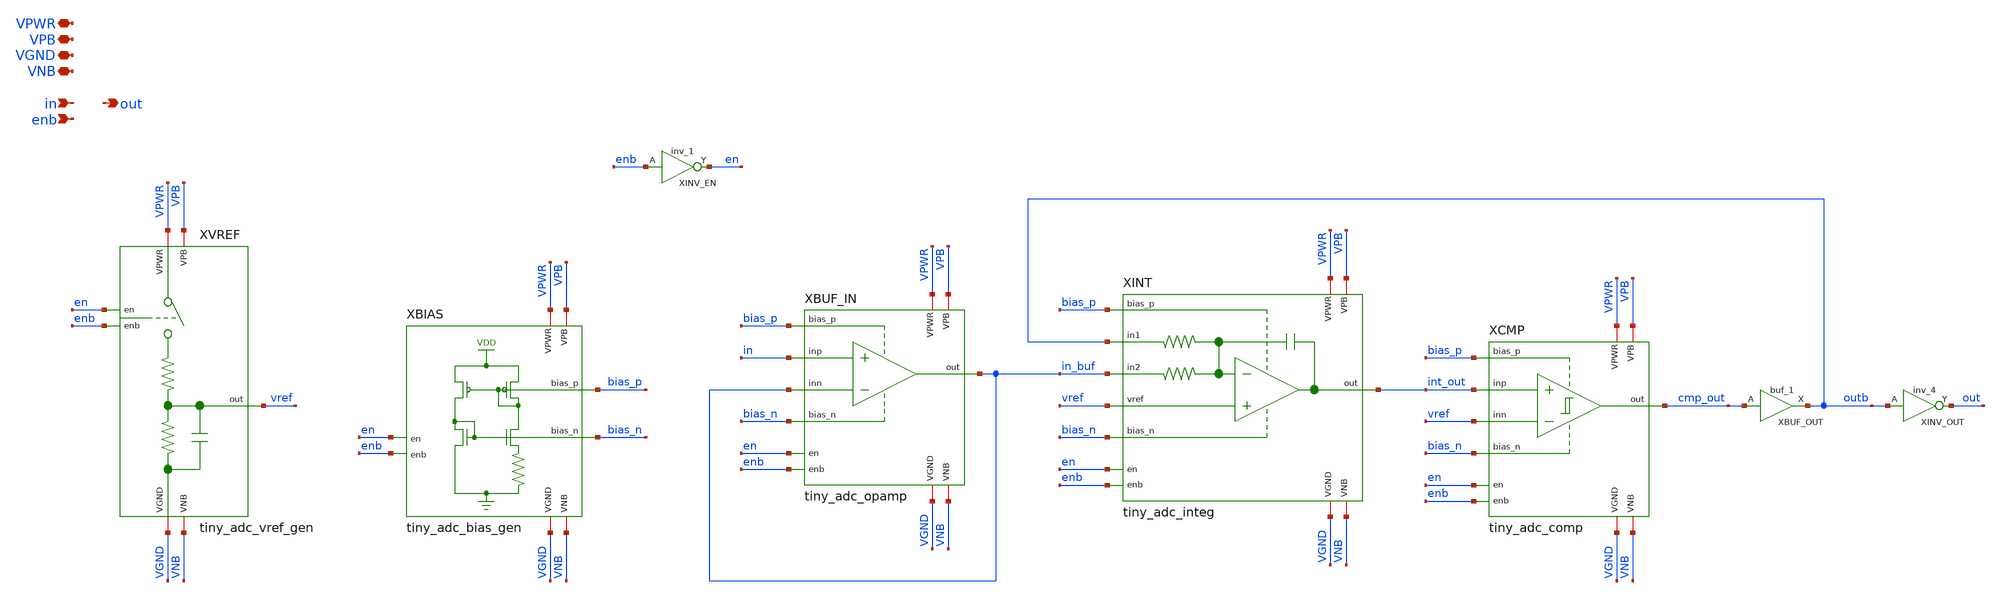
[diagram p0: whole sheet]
** sch_path: xschem/tiny_adc/tiny_adc.sch
**.subckt tiny_adc VNB VGND VPB VPWR out enb in
*.iopin VNB
*.iopin VGND
*.iopin VPB
*.iopin VPWR
*.opin out
*.ipin enb
*.ipin in
XCMP VPWR VPB VGND VNB int_out cmp_out vref bias_n bias_p en enb tiny_adc_comp
XBUF_IN VPWR VPB VGND VNB in in_buf in_buf bias_n bias_p en enb tiny_adc_opamp
XBUF_OUT cmp_out VGND VNB VPB VPWR outb sky130_fd_sc_hd__buf_1
XINV_OUT outb VGND VNB VPB VPWR out sky130_fd_sc_hd__inv_4
XINT VPWR VPB VGND VNB outb int_out in_buf bias_p bias_n vref en enb tiny_adc_integ
XBIAS VGND VNB VPWR VPB bias_n en enb bias_p tiny_adc_bias_gen
XVREF VGND VNB VPWR VPB vref en enb tiny_adc_vref_gen
XINV_EN enb VGND VNB VPB VPWR en sky130_fd_sc_hd__inv_1
**.ends
.end
